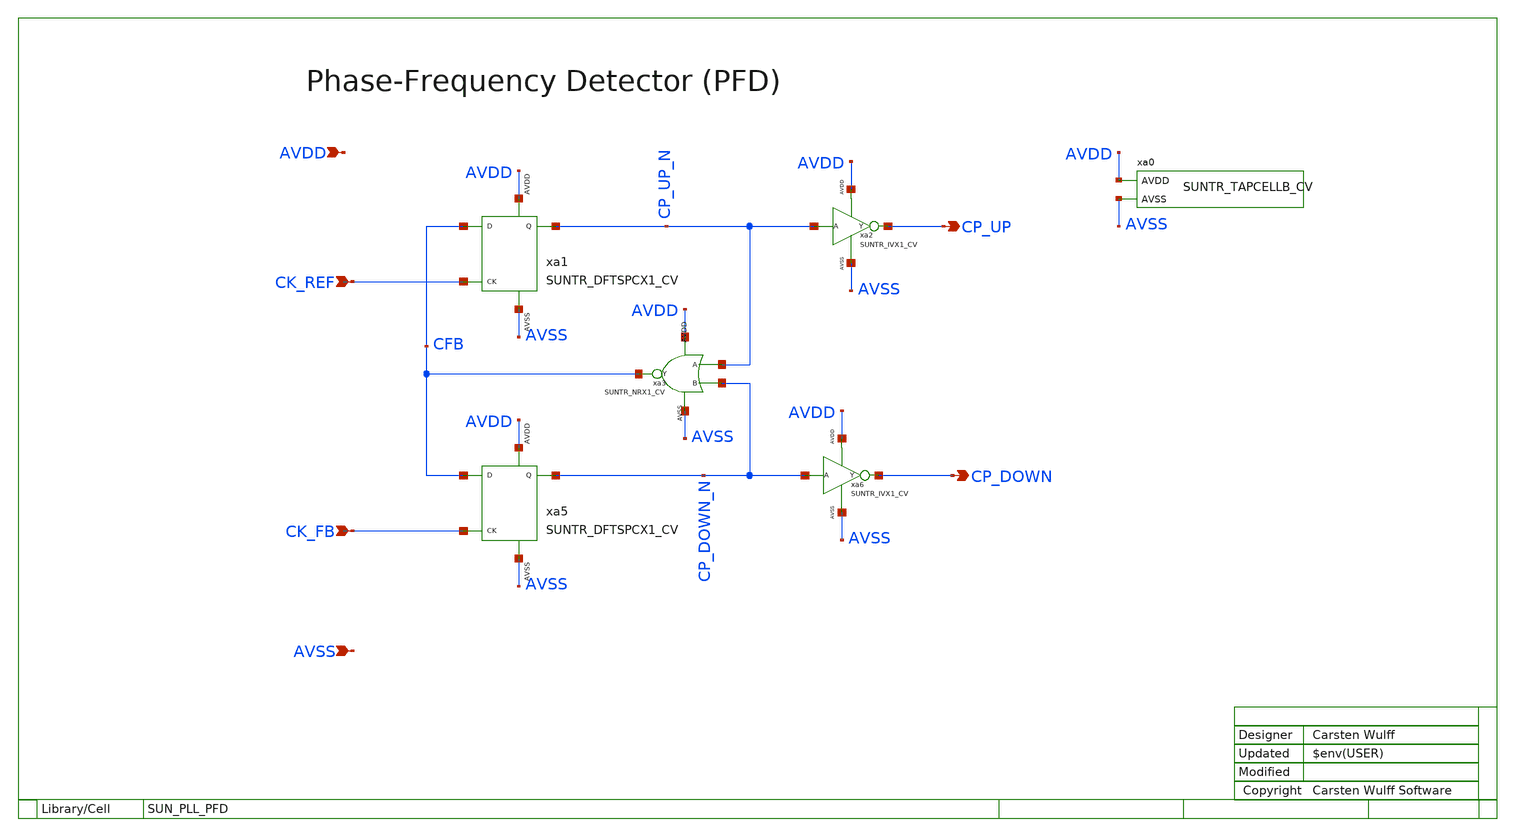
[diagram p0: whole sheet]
** sch_path: ip/sun_pll_sky130nm/design/SUN_PLL_SKY130NM/SUN_PLL_PFD.sch
**.subckt SUN_PLL_PFD CK_FB CK_REF CP_UP CP_DOWN AVDD AVSS
*.ipin CK_FB
*.ipin CK_REF
*.opin CP_UP
*.opin CP_DOWN
*.ipin AVDD
*.ipin AVSS
xa3 CP_UP_N CP_DOWN_N CFB AVDD AVSS SUNTR_NRX1_CV
xa2 CP_UP_N CP_UP AVDD AVSS SUNTR_IVX1_CV
xa6 CP_DOWN_N CP_DOWN AVDD AVSS SUNTR_IVX1_CV
xa1 CFB CK_REF CP_UP_N AVDD AVSS SUNTR_DFTSPCX1_CV
xa5 CFB CK_FB CP_DOWN_N AVDD AVSS SUNTR_DFTSPCX1_CV
xa0 AVDD AVSS SUNTR_TAPCELLB_CV
**.ends
.end
